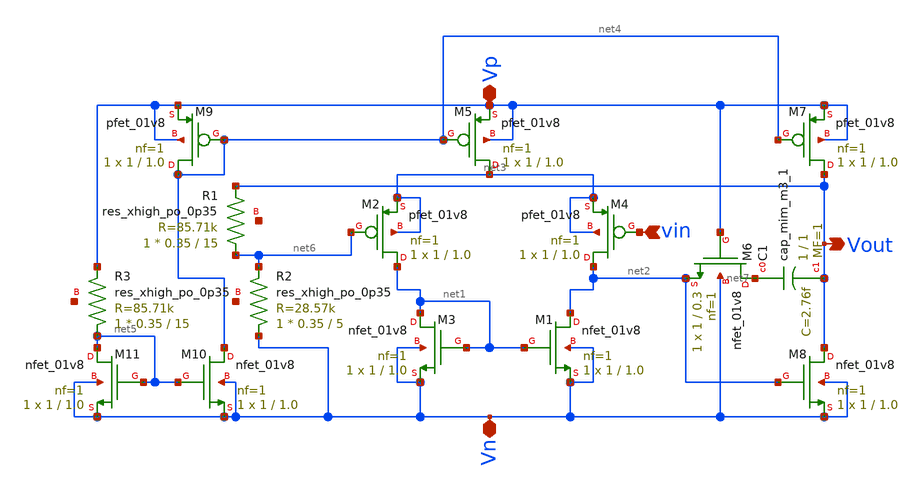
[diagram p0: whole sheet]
** sch_path: xschem/Vth_sch/Symbol/op-amp.sch
**.subckt op-amp vin Vp Vn Vout
*.ipin vin
*.iopin Vp
*.iopin Vn
*.opin Vout
XM1 net2 net1 Vn Vn sky130_fd_pr__nfet_01v8 L=1.0 W=1 nf=1 ad='int((nf+1)/2) * W/nf * 0.29' as='int((nf+2)/2) * W/nf * 0.29'
+ pd='2*int((nf+1)/2) * (W/nf + 0.29)' ps='2*int((nf+2)/2) * (W/nf + 0.29)' nrd='0.29 / W' nrs='0.29 / W'
+ sa=0 sb=0 sd=0 mult=1 m=1
XM2 net1 net6 net3 net3 sky130_fd_pr__pfet_01v8 L=1.0 W=1 nf=1 ad='int((nf+1)/2) * W/nf * 0.29' as='int((nf+2)/2) * W/nf * 0.29'
+ pd='2*int((nf+1)/2) * (W/nf + 0.29)' ps='2*int((nf+2)/2) * (W/nf + 0.29)' nrd='0.29 / W' nrs='0.29 / W'
+ sa=0 sb=0 sd=0 mult=1 m=1
XM3 net1 net1 Vn Vn sky130_fd_pr__nfet_01v8 L=1.0 W=1 nf=1 ad='int((nf+1)/2) * W/nf * 0.29' as='int((nf+2)/2) * W/nf * 0.29'
+ pd='2*int((nf+1)/2) * (W/nf + 0.29)' ps='2*int((nf+2)/2) * (W/nf + 0.29)' nrd='0.29 / W' nrs='0.29 / W'
+ sa=0 sb=0 sd=0 mult=1 m=1
XM4 net2 vin net3 net3 sky130_fd_pr__pfet_01v8 L=1.0 W=1 nf=1 ad='int((nf+1)/2) * W/nf * 0.29' as='int((nf+2)/2) * W/nf * 0.29'
+ pd='2*int((nf+1)/2) * (W/nf + 0.29)' ps='2*int((nf+2)/2) * (W/nf + 0.29)' nrd='0.29 / W' nrs='0.29 / W'
+ sa=0 sb=0 sd=0 mult=1 m=1
XM5 net3 net4 Vp Vp sky130_fd_pr__pfet_01v8 L=1.0 W=1 nf=1 ad='int((nf+1)/2) * W/nf * 0.29' as='int((nf+2)/2) * W/nf * 0.29'
+ pd='2*int((nf+1)/2) * (W/nf + 0.29)' ps='2*int((nf+2)/2) * (W/nf + 0.29)' nrd='0.29 / W' nrs='0.29 / W'
+ sa=0 sb=0 sd=0 mult=1 m=1
XM6 net7 Vp net2 Vn sky130_fd_pr__nfet_01v8 L=0.3 W=1 nf=1 ad='int((nf+1)/2) * W/nf * 0.29' as='int((nf+2)/2) * W/nf * 0.29'
+ pd='2*int((nf+1)/2) * (W/nf + 0.29)' ps='2*int((nf+2)/2) * (W/nf + 0.29)' nrd='0.29 / W' nrs='0.29 / W'
+ sa=0 sb=0 sd=0 mult=1 m=1
XC1 net7 Vout sky130_fd_pr__cap_mim_m3_1 W=1 L=1 MF=1 m=1
XM7 Vout net4 Vp Vp sky130_fd_pr__pfet_01v8 L=1.0 W=1 nf=1 ad='int((nf+1)/2) * W/nf * 0.29' as='int((nf+2)/2) * W/nf * 0.29'
+ pd='2*int((nf+1)/2) * (W/nf + 0.29)' ps='2*int((nf+2)/2) * (W/nf + 0.29)' nrd='0.29 / W' nrs='0.29 / W'
+ sa=0 sb=0 sd=0 mult=1 m=1
XM8 Vout net2 Vn Vn sky130_fd_pr__nfet_01v8 L=1.0 W=1 nf=1 ad='int((nf+1)/2) * W/nf * 0.29' as='int((nf+2)/2) * W/nf * 0.29'
+ pd='2*int((nf+1)/2) * (W/nf + 0.29)' ps='2*int((nf+2)/2) * (W/nf + 0.29)' nrd='0.29 / W' nrs='0.29 / W'
+ sa=0 sb=0 sd=0 mult=1 m=1
XM9 net4 net4 Vp Vp sky130_fd_pr__pfet_01v8 L=1.0 W=1 nf=1 ad='int((nf+1)/2) * W/nf * 0.29' as='int((nf+2)/2) * W/nf * 0.29'
+ pd='2*int((nf+1)/2) * (W/nf + 0.29)' ps='2*int((nf+2)/2) * (W/nf + 0.29)' nrd='0.29 / W' nrs='0.29 / W'
+ sa=0 sb=0 sd=0 mult=1 m=1
XM10 net4 net5 Vn Vn sky130_fd_pr__nfet_01v8 L=1.0 W=1 nf=1 ad='int((nf+1)/2) * W/nf * 0.29' as='int((nf+2)/2) * W/nf * 0.29'
+ pd='2*int((nf+1)/2) * (W/nf + 0.29)' ps='2*int((nf+2)/2) * (W/nf + 0.29)' nrd='0.29 / W' nrs='0.29 / W'
+ sa=0 sb=0 sd=0 mult=1 m=1
XM11 net5 net5 Vn Vn sky130_fd_pr__nfet_01v8 L=1.0 W=1 nf=1 ad='int((nf+1)/2) * W/nf * 0.29' as='int((nf+2)/2) * W/nf * 0.29'
+ pd='2*int((nf+1)/2) * (W/nf + 0.29)' ps='2*int((nf+2)/2) * (W/nf + 0.29)' nrd='0.29 / W' nrs='0.29 / W'
+ sa=0 sb=0 sd=0 mult=1 m=1
XR3 net5 Vp net8 sky130_fd_pr__res_xhigh_po_0p35 L=15 mult=1 m=1
XR1 net6 Vout net9 sky130_fd_pr__res_xhigh_po_0p35 L=15 mult=1 m=1
XR2 Vn net6 net10 sky130_fd_pr__res_xhigh_po_0p35 L=5 mult=1 m=1
**.ends
.end
